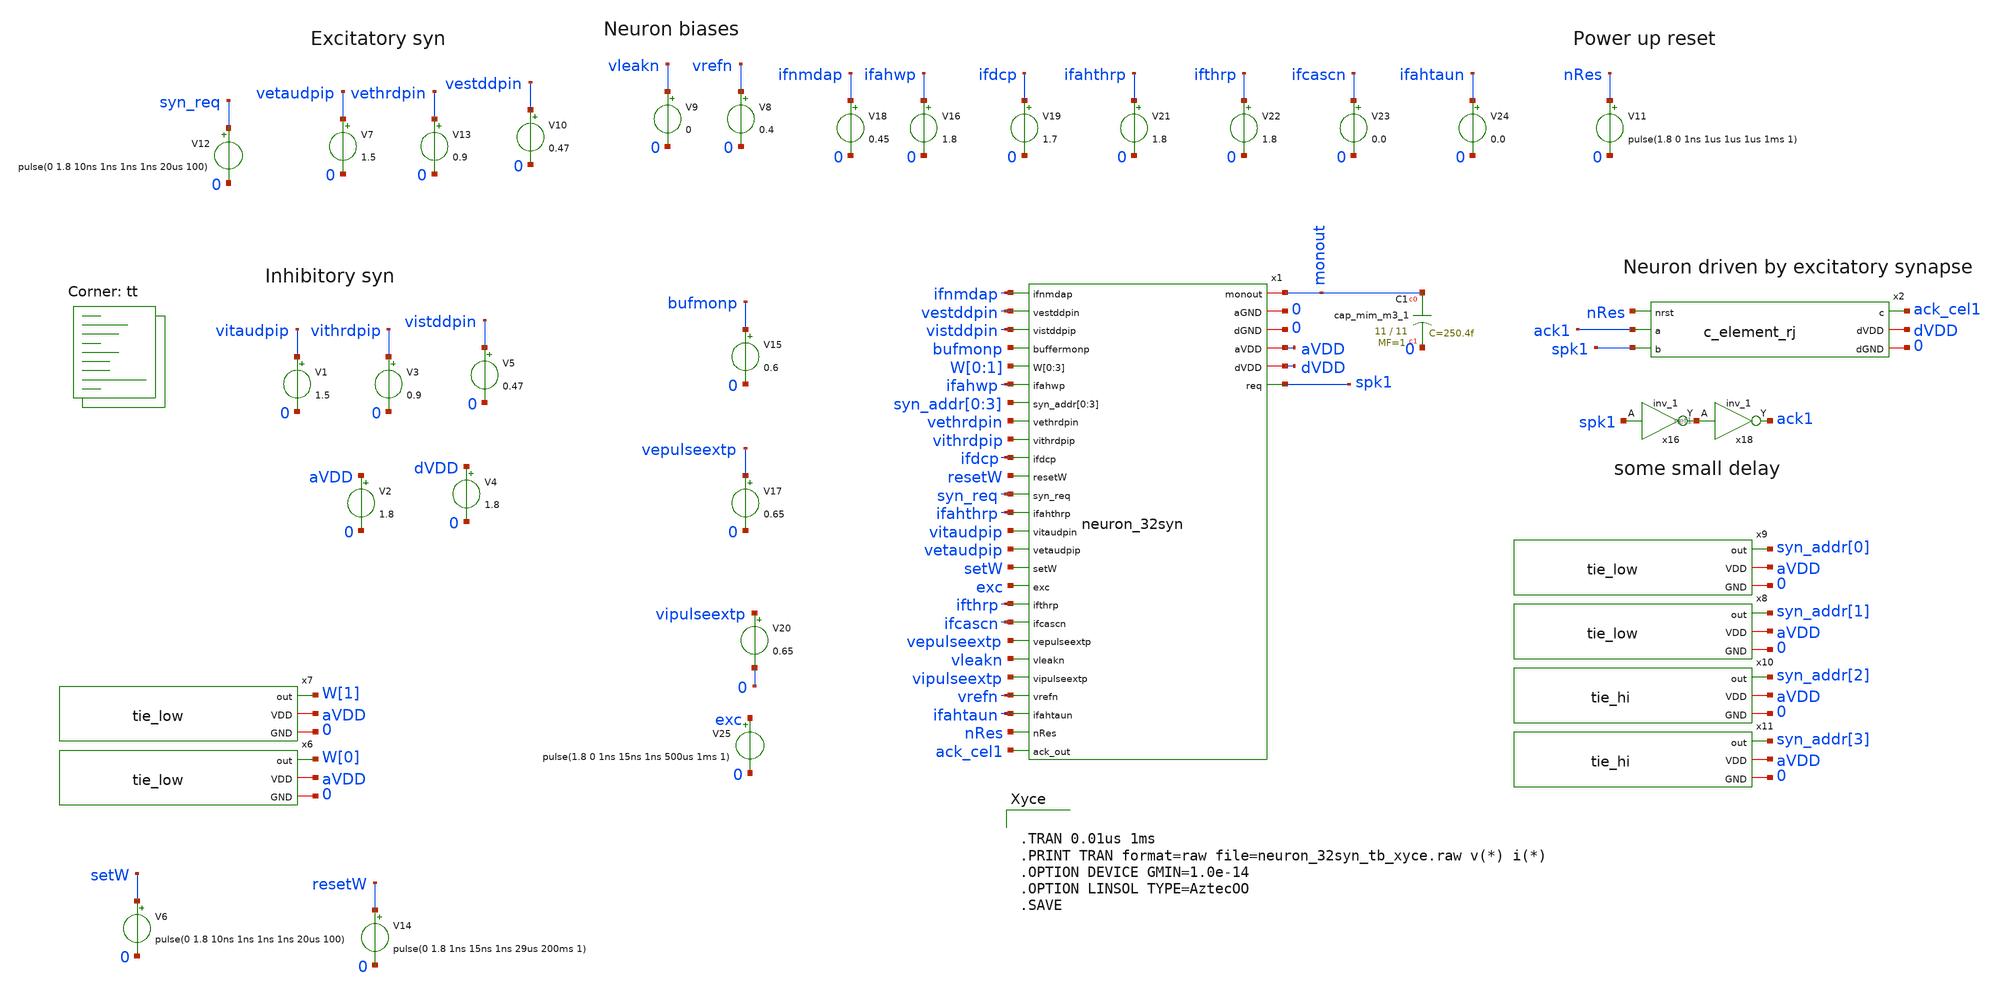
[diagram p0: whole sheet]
** sch_path: design/xschem/neuron_32syn_tb.sch
**.subckt neuron_32syn_tb
V2 aVDD 0 1.8
V8 vrefn 0 0.4
V9 vleakn 0 0
V16 ifahwp 0 1.8
V18 ifnmdap 0 0.45
V19 ifdcp 0 1.7
V21 ifahthrp 0 1.8
V22 ifthrp 0 1.8
V23 ifcascn 0 0.0
V24 ifahtaun 0 0.0
V7 vetaudpip 0 1.5
V13 vethrdpin 0 0.9
V10 vestddpin 0 0.47
V12 syn_req 0 pulse(0 1.8 10ns 1ns 1ns 1ns 20us 100)
V11 nRes 0 pulse(1.8 0 1ns 1us 1us 1us 1ms 1)
x1 ifnmdap vestddpin vistddpin bufmonp W[0] W[1] W[0] W[1] ifahwp syn_addr[0] syn_addr[1]
+ syn_addr[2] syn_addr[3] vethrdpin vithrdpip ifdcp monout resetW syn_req ifahthrp vitaudpip vetaudpip setW exc
+ ifthrp ifcascn vepulseextp vleakn vipulseextp 0 0 vrefn aVDD dVDD ifahtaun nRes ack_cel1 spk1 neuron_32syn
x2 nRes ack1 spk1 ack_cel1 dVDD 0 c_element_rj
V1 vitaudpip 0 1.5
V3 vithrdpip 0 0.9
V5 vistddpin 0 0.47
V15 bufmonp 0 0.6
x6 W[0] aVDD 0 tie_low
x7 W[1] aVDD 0 tie_low
V6 setW 0 pulse(0 1.8 10ns 1ns 1ns 1ns 20us 100)
V14 resetW 0 pulse(0 1.8 1ns 15ns 1ns 29us 200ms 1)
x8 syn_addr[1] aVDD 0 tie_low
x9 syn_addr[0] aVDD 0 tie_low
x10 syn_addr[2] aVDD 0 tie_hi
x11 syn_addr[3] aVDD 0 tie_hi
V17 vepulseextp 0 0.65
V20 vipulseextp 0 0.65
V25 exc 0 pulse(1.8 0 1ns 15ns 1ns 500us 1ms 1)
x16 spk1 0 0 dVDD dVDD net1 sky130_fd_sc_hd__inv_1
x18 net1 0 0 dVDD dVDD ack1 sky130_fd_sc_hd__inv_1
XC1 monout 0 sky130_fd_pr__cap_mim_m3_1 W=11 L=11 MF=1 m=1
V4 dVDD 0 1.8
**** begin user architecture code


* Standard cell simulation files
.include $::SKYWATER_STDCELLS/sky130_fd_sc_hd.spice




.TRAN 0.01us 1ms
.PRINT TRAN format=raw file=neuron_32syn_tb_xyce.raw v(*) i(*)
.OPTION DEVICE GMIN=1.0e-14
.OPTION LINSOL TYPE=AztecOO
.SAVE



.lib $::SKYWATER_MODELS/sky130.lib.spice tt
**** end user architecture code
**.ends

* expanding   symbol:  neuron_32syn.sym # of pins=32
** sym_path: design/xschem/neuron_32syn.sym
** sch_path: design/xschem/neuron_32syn.sch
.subckt neuron_32syn ifnmdap vestddpin vistddpip buffermonp W[0] W[1] W[2] W[3] ifahwp syn_addr[0]
+ syn_addr[1] syn_addr[2] syn_addr[3] vethrdpin vithrdpip ifdcp monout resetW syn_req ifahthrp vitaudpin
+ vetaudpip setW exc ifthrp ifcascn vepulseextp vleakn vipulseextp aGND dGND vrefn aVDD dVDD ifahtaun nRes
+ ack_out req
*.ipin ack_out
*.iopin dGND
*.iopin dVDD
*.ipin vepulseextp
*.ipin syn_addr[0],syn_addr[1],syn_addr[2],syn_addr[3]
*.ipin W[0],W[1],W[2],W[3]
*.ipin vethrdpin
*.ipin vetaudpip
*.ipin vestddpin
*.ipin setW
*.ipin resetW
*.ipin syn_req
*.ipin exc
*.ipin vithrdpip
*.ipin vitaudpin
*.ipin vistddpip
*.ipin vipulseextp
*.opin req
*.ipin vleakn
*.ipin ifdcp
*.ipin ifthrp
*.ipin ifahwp
*.ipin ifahthrp
*.ipin ifahtaun
*.ipin ifcascn
*.ipin vrefn
*.ipin ifnmdap
*.ipin nRes
*.iopin aGND
*.iopin aVDD
*.ipin buffermonp
*.iopin monout
x1 vestddpin net1 W[0] W[1] W[2] W[3] syn_addr[0] syn_addr[1] syn_addr[2] syn_addr[3] vethrdpin
+ resetWe reqe vetaudpip setWe vepulseextp aGND aVDD synapse_array_programmable_16_to_sout
x2 vistddpip net1 W[0] W[1] W[2] W[3] syn_addr[0] syn_addr[1] syn_addr[2] syn_addr[3] vithrdpip
+ resetWi reqi vitaudpin setWi vipulseextp aGND aVDD synapse_array_programmable_inh_16_to_sout
x3 nreq_neu1 net1 net2 ifahwp ifnmdap ifahthrp net3 ifdcp ifthrp ifcascn vleakn vrefn ifahtaun aGND
+ aVDD neuron_analog_fc
x11 nRes req ack_out ack_cel1 dVDD dGND c_element_rj
x4 setW exc dGND dGND dVDD dVDD setWe sky130_fd_sc_hd__and2_1
x5 exc dGND dGND dVDD dVDD nExc sky130_fd_sc_hd__inv_1
x6 setW nExc dGND dGND dVDD dVDD setWi sky130_fd_sc_hd__and2_1
x7 resetW exc dGND dGND dVDD dVDD resetWe sky130_fd_sc_hd__and2_1
x8 resetW nExc dGND dGND dVDD dVDD resetWi sky130_fd_sc_hd__and2_1
x10 syn_req exc dGND dGND dVDD dVDD reqe sky130_fd_sc_hd__and2_1
x12 syn_req nExc dGND dGND dVDD dVDD reqi sky130_fd_sc_hd__and2_1
x13 monout buffermonp net3 aGND aVDD buffer_mon
x14 ack_cel1 dGND dGND dVDD dVDD net2 sky130_fd_sc_hd__inv_1
x15 nreq_neu1 req dVDD dGND schmitt_trigger
.ends


* expanding   symbol:  c_element_rj.sym # of pins=6
** sym_path: design/xschem/c_element_rj.sym
** sch_path: design/xschem/c_element_rj.sch
.subckt c_element_rj nrst a b c dVDD dGND
*.iopin dGND
*.iopin dVDD
*.opin c
*.ipin b
*.ipin a
*.ipin nrst
XM14 c net6 dVDD dVDD sky130_fd_pr__pfet_01v8 L=0.15 W=1 nf=1 ad='int((nf+1)/2) * W/nf * 0.29' as='int((nf+2)/2) * W/nf * 0.29'
+ pd='2*int((nf+1)/2) * (W/nf + 0.29)' ps='2*int((nf+2)/2) * (W/nf + 0.29)' nrd='0.29 / W' nrs='0.29 / W'
+ sa=0 sb=0 sd=0 mult=1 m=1
XM5 net6 nrst dVDD dVDD sky130_fd_pr__pfet_01v8 L=0.15 W=1 nf=1 ad='int((nf+1)/2) * W/nf * 0.29' as='int((nf+2)/2) * W/nf * 0.29'
+ pd='2*int((nf+1)/2) * (W/nf + 0.29)' ps='2*int((nf+2)/2) * (W/nf + 0.29)' nrd='0.29 / W' nrs='0.29 / W'
+ sa=0 sb=0 sd=0 mult=1 m=1
XM6 net5 b dVDD dVDD sky130_fd_pr__pfet_01v8 L=0.15 W=1 nf=1 ad='int((nf+1)/2) * W/nf * 0.29' as='int((nf+2)/2) * W/nf * 0.29'
+ pd='2*int((nf+1)/2) * (W/nf + 0.29)' ps='2*int((nf+2)/2) * (W/nf + 0.29)' nrd='0.29 / W' nrs='0.29 / W'
+ sa=0 sb=0 sd=0 mult=1 m=1
XM4 net4 a dVDD dVDD sky130_fd_pr__pfet_01v8 L=0.15 W=1 nf=1 ad='int((nf+1)/2) * W/nf * 0.29' as='int((nf+2)/2) * W/nf * 0.29'
+ pd='2*int((nf+1)/2) * (W/nf + 0.29)' ps='2*int((nf+2)/2) * (W/nf + 0.29)' nrd='0.29 / W' nrs='0.29 / W'
+ sa=0 sb=0 sd=0 mult=1 m=1
XM7 net3 b net4 dVDD sky130_fd_pr__pfet_01v8 L=0.15 W=1 nf=1 ad='int((nf+1)/2) * W/nf * 0.29' as='int((nf+2)/2) * W/nf * 0.29'
+ pd='2*int((nf+1)/2) * (W/nf + 0.29)' ps='2*int((nf+2)/2) * (W/nf + 0.29)' nrd='0.29 / W' nrs='0.29 / W'
+ sa=0 sb=0 sd=0 mult=1 m=1
XM8 net3 a net5 dVDD sky130_fd_pr__pfet_01v8 L=0.15 W=1 nf=1 ad='int((nf+1)/2) * W/nf * 0.29' as='int((nf+2)/2) * W/nf * 0.29'
+ pd='2*int((nf+1)/2) * (W/nf + 0.29)' ps='2*int((nf+2)/2) * (W/nf + 0.29)' nrd='0.29 / W' nrs='0.29 / W'
+ sa=0 sb=0 sd=0 mult=1 m=1
XM10 net5 c net4 dVDD sky130_fd_pr__pfet_01v8 L=0.15 W=1 nf=1 ad='int((nf+1)/2) * W/nf * 0.29' as='int((nf+2)/2) * W/nf * 0.29'
+ pd='2*int((nf+1)/2) * (W/nf + 0.29)' ps='2*int((nf+2)/2) * (W/nf + 0.29)' nrd='0.29 / W' nrs='0.29 / W'
+ sa=0 sb=0 sd=0 mult=1 m=1
XM12 c net6 dGND dGND sky130_fd_pr__nfet_01v8 L=0.15 W=0.65 nf=1 ad='int((nf+1)/2) * W/nf * 0.29' as='int((nf+2)/2) * W/nf * 0.29'
+ pd='2*int((nf+1)/2) * (W/nf + 0.29)' ps='2*int((nf+2)/2) * (W/nf + 0.29)' nrd='0.29 / W' nrs='0.29 / W'
+ sa=0 sb=0 sd=0 mult=1 m=1
XM1 net3 nrst net6 dGND sky130_fd_pr__nfet_01v8 L=0.15 W=0.65 nf=1 ad='int((nf+1)/2) * W/nf * 0.29' as='int((nf+2)/2) * W/nf * 0.29'
+ pd='2*int((nf+1)/2) * (W/nf + 0.29)' ps='2*int((nf+2)/2) * (W/nf + 0.29)' nrd='0.29 / W' nrs='0.29 / W'
+ sa=0 sb=0 sd=0 mult=1 m=1
XM2 net3 b net1 dGND sky130_fd_pr__nfet_01v8 L=0.15 W=0.65 nf=1 ad='int((nf+1)/2) * W/nf * 0.29' as='int((nf+2)/2) * W/nf * 0.29'
+ pd='2*int((nf+1)/2) * (W/nf + 0.29)' ps='2*int((nf+2)/2) * (W/nf + 0.29)' nrd='0.29 / W' nrs='0.29 / W'
+ sa=0 sb=0 sd=0 mult=1 m=1
XM3 net3 a net2 dGND sky130_fd_pr__nfet_01v8 L=0.15 W=0.65 nf=1 ad='int((nf+1)/2) * W/nf * 0.29' as='int((nf+2)/2) * W/nf * 0.29'
+ pd='2*int((nf+1)/2) * (W/nf + 0.29)' ps='2*int((nf+2)/2) * (W/nf + 0.29)' nrd='0.29 / W' nrs='0.29 / W'
+ sa=0 sb=0 sd=0 mult=1 m=1
XM9 net2 c net1 dGND sky130_fd_pr__nfet_01v8 L=0.15 W=0.65 nf=1 ad='int((nf+1)/2) * W/nf * 0.29' as='int((nf+2)/2) * W/nf * 0.29'
+ pd='2*int((nf+1)/2) * (W/nf + 0.29)' ps='2*int((nf+2)/2) * (W/nf + 0.29)' nrd='0.29 / W' nrs='0.29 / W'
+ sa=0 sb=0 sd=0 mult=1 m=1
XM11 net1 a dGND dGND sky130_fd_pr__nfet_01v8 L=0.15 W=0.65 nf=1 ad='int((nf+1)/2) * W/nf * 0.29' as='int((nf+2)/2) * W/nf * 0.29'
+ pd='2*int((nf+1)/2) * (W/nf + 0.29)' ps='2*int((nf+2)/2) * (W/nf + 0.29)' nrd='0.29 / W' nrs='0.29 / W'
+ sa=0 sb=0 sd=0 mult=1 m=1
XM13 net2 b dGND dGND sky130_fd_pr__nfet_01v8 L=0.15 W=0.65 nf=1 ad='int((nf+1)/2) * W/nf * 0.29' as='int((nf+2)/2) * W/nf * 0.29'
+ pd='2*int((nf+1)/2) * (W/nf + 0.29)' ps='2*int((nf+2)/2) * (W/nf + 0.29)' nrd='0.29 / W' nrs='0.29 / W'
+ sa=0 sb=0 sd=0 mult=1 m=1
.ends


* expanding   symbol:  tie_low.sym # of pins=3
** sym_path: design/xschem/tie_low.sym
** sch_path: design/xschem/tie_low.sch
.subckt tie_low out VDD GND
*.iopin VDD
*.iopin GND
*.opin out
XM4 net1 net1 VDD VDD sky130_fd_pr__pfet_01v8 L=0.15 W=1 nf=1 ad='int((nf+1)/2) * W/nf * 0.29' as='int((nf+2)/2) * W/nf * 0.29'
+ pd='2*int((nf+1)/2) * (W/nf + 0.29)' ps='2*int((nf+2)/2) * (W/nf + 0.29)' nrd='0.29 / W' nrs='0.29 / W'
+ sa=0 sb=0 sd=0 mult=1 m=1
XM2 out net1 GND GND sky130_fd_pr__nfet_01v8 L=0.15 W=0.65 nf=1 ad='int((nf+1)/2) * W/nf * 0.29' as='int((nf+2)/2) * W/nf * 0.29'
+ pd='2*int((nf+1)/2) * (W/nf + 0.29)' ps='2*int((nf+2)/2) * (W/nf + 0.29)' nrd='0.29 / W' nrs='0.29 / W'
+ sa=0 sb=0 sd=0 mult=1 m=1
.ends


* expanding   symbol:  tie_hi.sym # of pins=3
** sym_path: design/xschem/tie_hi.sym
** sch_path: design/xschem/tie_hi.sch
.subckt tie_hi out VDD GND
*.iopin VDD
*.iopin GND
*.opin out
XM4 out net1 VDD VDD sky130_fd_pr__pfet_01v8 L=0.15 W=1 nf=1 ad='int((nf+1)/2) * W/nf * 0.29' as='int((nf+2)/2) * W/nf * 0.29'
+ pd='2*int((nf+1)/2) * (W/nf + 0.29)' ps='2*int((nf+2)/2) * (W/nf + 0.29)' nrd='0.29 / W' nrs='0.29 / W'
+ sa=0 sb=0 sd=0 mult=1 m=1
XM2 net1 net1 GND GND sky130_fd_pr__nfet_01v8 L=0.15 W=0.65 nf=1 ad='int((nf+1)/2) * W/nf * 0.29' as='int((nf+2)/2) * W/nf * 0.29'
+ pd='2*int((nf+1)/2) * (W/nf + 0.29)' ps='2*int((nf+2)/2) * (W/nf + 0.29)' nrd='0.29 / W' nrs='0.29 / W'
+ sa=0 sb=0 sd=0 mult=1 m=1
.ends


* expanding   symbol:  synapse_array_programmable_16_to_sout.sym # of pins=12
** sym_path: design/xschem/synapse_array_programmable_16_to_sout.sym
** sch_path: design/xschem/synapse_array_programmable_16_to_sout.sch
.subckt synapse_array_programmable_16_to_sout vstddpin sout W[0] W[1] W[2] W[3] syn_addr[0]
+ syn_addr[1] syn_addr[2] syn_addr[3] vthrdpin resetW req vtaudpip setW vpulseextp GND VDD
*.iopin GND
*.iopin VDD
*.ipin vpulseextp
*.ipin syn_addr[0],syn_addr[1],syn_addr[2],syn_addr[3]
*.ipin W[0],W[1],W[2],W[3]
*.ipin vthrdpin
*.ipin vtaudpip
*.ipin vstddpin
*.iopin sout
*.ipin setW
*.ipin resetW
*.ipin req
x1[0] sout vstddpin net1[15] resetW vthrdpin setW vtaudpip W[0] W[1] W[2] W[3] vpulseextp GND VDD
+ synapse_4bit_memory
x1[1] sout vstddpin net1[14] resetW vthrdpin setW vtaudpip W[0] W[1] W[2] W[3] vpulseextp GND VDD
+ synapse_4bit_memory
x1[2] sout vstddpin net1[13] resetW vthrdpin setW vtaudpip W[0] W[1] W[2] W[3] vpulseextp GND VDD
+ synapse_4bit_memory
x1[3] sout vstddpin net1[12] resetW vthrdpin setW vtaudpip W[0] W[1] W[2] W[3] vpulseextp GND VDD
+ synapse_4bit_memory
x1[4] sout vstddpin net1[11] resetW vthrdpin setW vtaudpip W[0] W[1] W[2] W[3] vpulseextp GND VDD
+ synapse_4bit_memory
x1[5] sout vstddpin net1[10] resetW vthrdpin setW vtaudpip W[0] W[1] W[2] W[3] vpulseextp GND VDD
+ synapse_4bit_memory
x1[6] sout vstddpin net1[9] resetW vthrdpin setW vtaudpip W[0] W[1] W[2] W[3] vpulseextp GND VDD
+ synapse_4bit_memory
x1[7] sout vstddpin net1[8] resetW vthrdpin setW vtaudpip W[0] W[1] W[2] W[3] vpulseextp GND VDD
+ synapse_4bit_memory
x1[8] sout vstddpin net1[7] resetW vthrdpin setW vtaudpip W[0] W[1] W[2] W[3] vpulseextp GND VDD
+ synapse_4bit_memory
x1[9] sout vstddpin net1[6] resetW vthrdpin setW vtaudpip W[0] W[1] W[2] W[3] vpulseextp GND VDD
+ synapse_4bit_memory
x1[10] sout vstddpin net1[5] resetW vthrdpin setW vtaudpip W[0] W[1] W[2] W[3] vpulseextp GND VDD
+ synapse_4bit_memory
x1[11] sout vstddpin net1[4] resetW vthrdpin setW vtaudpip W[0] W[1] W[2] W[3] vpulseextp GND VDD
+ synapse_4bit_memory
x1[12] sout vstddpin net1[3] resetW vthrdpin setW vtaudpip W[0] W[1] W[2] W[3] vpulseextp GND VDD
+ synapse_4bit_memory
x1[13] sout vstddpin net1[2] resetW vthrdpin setW vtaudpip W[0] W[1] W[2] W[3] vpulseextp GND VDD
+ synapse_4bit_memory
x1[14] sout vstddpin net1[1] resetW vthrdpin setW vtaudpip W[0] W[1] W[2] W[3] vpulseextp GND VDD
+ synapse_4bit_memory
x1[15] sout vstddpin net1[0] resetW vthrdpin setW vtaudpip W[0] W[1] W[2] W[3] vpulseextp GND VDD
+ synapse_4bit_memory
x3 syn_addr[0] syn_addr[1] syn_addr[2] syn_addr[3] D[15] D[14] D[13] D[12] D[11] D[10] D[9] D[8]
+ D[7] D[6] D[5] D[4] D[3] D[2] D[1] D[0] req req_syn VDD GND decoder_4_to_16
x4[0] D[0] req_syn GND GND VDD VDD net1[15] sky130_fd_sc_hd__and2_1
x4[1] D[1] req_syn GND GND VDD VDD net1[14] sky130_fd_sc_hd__and2_1
x4[2] D[2] req_syn GND GND VDD VDD net1[13] sky130_fd_sc_hd__and2_1
x4[3] D[3] req_syn GND GND VDD VDD net1[12] sky130_fd_sc_hd__and2_1
x4[4] D[4] req_syn GND GND VDD VDD net1[11] sky130_fd_sc_hd__and2_1
x4[5] D[5] req_syn GND GND VDD VDD net1[10] sky130_fd_sc_hd__and2_1
x4[6] D[6] req_syn GND GND VDD VDD net1[9] sky130_fd_sc_hd__and2_1
x4[7] D[7] req_syn GND GND VDD VDD net1[8] sky130_fd_sc_hd__and2_1
x4[8] D[8] req_syn GND GND VDD VDD net1[7] sky130_fd_sc_hd__and2_1
x4[9] D[9] req_syn GND GND VDD VDD net1[6] sky130_fd_sc_hd__and2_1
x4[10] D[10] req_syn GND GND VDD VDD net1[5] sky130_fd_sc_hd__and2_1
x4[11] D[11] req_syn GND GND VDD VDD net1[4] sky130_fd_sc_hd__and2_1
x4[12] D[12] req_syn GND GND VDD VDD net1[3] sky130_fd_sc_hd__and2_1
x4[13] D[13] req_syn GND GND VDD VDD net1[2] sky130_fd_sc_hd__and2_1
x4[14] D[14] req_syn GND GND VDD VDD net1[1] sky130_fd_sc_hd__and2_1
x4[15] D[15] req_syn GND GND VDD VDD net1[0] sky130_fd_sc_hd__and2_1
.ends


* expanding   symbol:  synapse_array_programmable_inh_16_to_sout.sym # of pins=12
** sym_path: design/xschem/synapse_array_programmable_inh_16_to_sout.sym
** sch_path: design/xschem/synapse_array_programmable_inh_16_to_sout.sch
.subckt synapse_array_programmable_inh_16_to_sout vstddpip sout W[0] W[1] W[2] W[3] syn_addr[0]
+ syn_addr[1] syn_addr[2] syn_addr[3] vthrdpip resetW req vtaudpin setW vpulseextp GND VDD
*.iopin GND
*.iopin VDD
*.ipin vpulseextp
*.ipin syn_addr[0],syn_addr[1],syn_addr[2],syn_addr[3]
*.ipin W[0],W[1],W[2],W[3]
*.ipin vthrdpip
*.ipin vtaudpin
*.ipin vstddpip
*.iopin sout
*.ipin setW
*.ipin resetW
*.ipin req
x3 syn_addr[0] syn_addr[1] syn_addr[2] syn_addr[3] D[15] D[14] D[13] D[12] D[11] D[10] D[9] D[8]
+ D[7] D[6] D[5] D[4] D[3] D[2] D[1] D[0] req req_syn VDD GND decoder_4_to_16
x4[0] D[0] req_syn GND GND VDD VDD net1[15] sky130_fd_sc_hd__and2_1
x4[1] D[1] req_syn GND GND VDD VDD net1[14] sky130_fd_sc_hd__and2_1
x4[2] D[2] req_syn GND GND VDD VDD net1[13] sky130_fd_sc_hd__and2_1
x4[3] D[3] req_syn GND GND VDD VDD net1[12] sky130_fd_sc_hd__and2_1
x4[4] D[4] req_syn GND GND VDD VDD net1[11] sky130_fd_sc_hd__and2_1
x4[5] D[5] req_syn GND GND VDD VDD net1[10] sky130_fd_sc_hd__and2_1
x4[6] D[6] req_syn GND GND VDD VDD net1[9] sky130_fd_sc_hd__and2_1
x4[7] D[7] req_syn GND GND VDD VDD net1[8] sky130_fd_sc_hd__and2_1
x4[8] D[8] req_syn GND GND VDD VDD net1[7] sky130_fd_sc_hd__and2_1
x4[9] D[9] req_syn GND GND VDD VDD net1[6] sky130_fd_sc_hd__and2_1
x4[10] D[10] req_syn GND GND VDD VDD net1[5] sky130_fd_sc_hd__and2_1
x4[11] D[11] req_syn GND GND VDD VDD net1[4] sky130_fd_sc_hd__and2_1
x4[12] D[12] req_syn GND GND VDD VDD net1[3] sky130_fd_sc_hd__and2_1
x4[13] D[13] req_syn GND GND VDD VDD net1[2] sky130_fd_sc_hd__and2_1
x4[14] D[14] req_syn GND GND VDD VDD net1[1] sky130_fd_sc_hd__and2_1
x4[15] D[15] req_syn GND GND VDD VDD net1[0] sky130_fd_sc_hd__and2_1
x1[0] sout vstddpip net1[15] resetW vthrdpip setW vtaudpin W[0] W[1] W[2] W[3] vpulseextp GND VDD
+ synapse_4bit_memory_inh
x1[1] sout vstddpip net1[14] resetW vthrdpip setW vtaudpin W[0] W[1] W[2] W[3] vpulseextp GND VDD
+ synapse_4bit_memory_inh
x1[2] sout vstddpip net1[13] resetW vthrdpip setW vtaudpin W[0] W[1] W[2] W[3] vpulseextp GND VDD
+ synapse_4bit_memory_inh
x1[3] sout vstddpip net1[12] resetW vthrdpip setW vtaudpin W[0] W[1] W[2] W[3] vpulseextp GND VDD
+ synapse_4bit_memory_inh
x1[4] sout vstddpip net1[11] resetW vthrdpip setW vtaudpin W[0] W[1] W[2] W[3] vpulseextp GND VDD
+ synapse_4bit_memory_inh
x1[5] sout vstddpip net1[10] resetW vthrdpip setW vtaudpin W[0] W[1] W[2] W[3] vpulseextp GND VDD
+ synapse_4bit_memory_inh
x1[6] sout vstddpip net1[9] resetW vthrdpip setW vtaudpin W[0] W[1] W[2] W[3] vpulseextp GND VDD
+ synapse_4bit_memory_inh
x1[7] sout vstddpip net1[8] resetW vthrdpip setW vtaudpin W[0] W[1] W[2] W[3] vpulseextp GND VDD
+ synapse_4bit_memory_inh
x1[8] sout vstddpip net1[7] resetW vthrdpip setW vtaudpin W[0] W[1] W[2] W[3] vpulseextp GND VDD
+ synapse_4bit_memory_inh
x1[9] sout vstddpip net1[6] resetW vthrdpip setW vtaudpin W[0] W[1] W[2] W[3] vpulseextp GND VDD
+ synapse_4bit_memory_inh
x1[10] sout vstddpip net1[5] resetW vthrdpip setW vtaudpin W[0] W[1] W[2] W[3] vpulseextp GND VDD
+ synapse_4bit_memory_inh
x1[11] sout vstddpip net1[4] resetW vthrdpip setW vtaudpin W[0] W[1] W[2] W[3] vpulseextp GND VDD
+ synapse_4bit_memory_inh
x1[12] sout vstddpip net1[3] resetW vthrdpip setW vtaudpin W[0] W[1] W[2] W[3] vpulseextp GND VDD
+ synapse_4bit_memory_inh
x1[13] sout vstddpip net1[2] resetW vthrdpip setW vtaudpin W[0] W[1] W[2] W[3] vpulseextp GND VDD
+ synapse_4bit_memory_inh
x1[14] sout vstddpip net1[1] resetW vthrdpip setW vtaudpin W[0] W[1] W[2] W[3] vpulseextp GND VDD
+ synapse_4bit_memory_inh
x1[15] sout vstddpip net1[0] resetW vthrdpip setW vtaudpin W[0] W[1] W[2] W[3] vpulseextp GND VDD
+ synapse_4bit_memory_inh
.ends


* expanding   symbol:  neuron_analog_fc.sym # of pins=15
** sym_path: design/xschem/neuron_analog_fc.sym
** sch_path: design/xschem/neuron_analog_fc.sch
.subckt neuron_analog_fc nreq sinp nack ifahwp ifnmdap ifahthrp vmem ifdcp ifthrp ifcascn vleakn
+ vrefn ifahtaun GND VDD
*.ipin vleakn
*.iopin GND
*.iopin VDD
*.opin nreq
*.ipin vrefn
*.ipin nack
*.ipin ifdcp
*.ipin ifthrp
*.ipin ifnmdap
*.ipin ifahwp
*.ipin ifahthrp
*.ipin ifahtaun
*.ipin ifcascn
*.iopin vmem
*.iopin sinp
XC1 GND vmem sky130_fd_pr__cap_mim_m3_1 W=11 L=11 MF=1 m=1
XM8 net4 vrefn GND GND sky130_fd_pr__nfet_01v8 L=0.25 W=0.8 nf=1 ad='int((nf+1)/2) * W/nf * 0.29' as='int((nf+2)/2) * W/nf * 0.29'
+ pd='2*int((nf+1)/2) * (W/nf + 0.29)' ps='2*int((nf+2)/2) * (W/nf + 0.29)' nrd='0.29 / W' nrs='0.29 / W'
+ sa=0 sb=0 sd=0 mult=1 m=1
XM9 net5 nack VDD VDD sky130_fd_pr__pfet_01v8 L=0.2 W=1.2 nf=1 ad='int((nf+1)/2) * W/nf * 0.29' as='int((nf+2)/2) * W/nf * 0.29'
+ pd='2*int((nf+1)/2) * (W/nf + 0.29)' ps='2*int((nf+2)/2) * (W/nf + 0.29)' nrd='0.29 / W' nrs='0.29 / W'
+ sa=0 sb=0 sd=0 mult=1 m=1
XC2 GND net3 sky130_fd_pr__cap_mim_m3_1 W=4 L=2 MF=1 m=1
XM21 vmem net3 GND GND sky130_fd_pr__nfet_01v8 L=0.25 W=1 nf=1 ad='int((nf+1)/2) * W/nf * 0.29' as='int((nf+2)/2) * W/nf * 0.29'
+ pd='2*int((nf+1)/2) * (W/nf + 0.29)' ps='2*int((nf+2)/2) * (W/nf + 0.29)' nrd='0.29 / W' nrs='0.29 / W'
+ sa=0 sb=0 sd=0 mult=1 m=1
XM15 net12 ifnmdap sinp VDD sky130_fd_pr__pfet_01v8 L=0.15 W=1 nf=1 ad='int((nf+1)/2) * W/nf * 0.29'
+ as='int((nf+2)/2) * W/nf * 0.29' pd='2*int((nf+1)/2) * (W/nf + 0.29)' ps='2*int((nf+2)/2) * (W/nf + 0.29)'
+ nrd='0.29 / W' nrs='0.29 / W' sa=0 sb=0 sd=0 mult=1 m=1
XC3 GND net8 sky130_fd_pr__cap_mim_m3_1 W=5 L=5 MF=1 m=1
XM12 GND vmem sinp VDD sky130_fd_pr__pfet_01v8 L=0.15 W=1 nf=1 ad='int((nf+1)/2) * W/nf * 0.29' as='int((nf+2)/2) * W/nf * 0.29'
+ pd='2*int((nf+1)/2) * (W/nf + 0.29)' ps='2*int((nf+2)/2) * (W/nf + 0.29)' nrd='0.29 / W' nrs='0.29 / W'
+ sa=0 sb=0 sd=0 mult=1 m=1
XM11 GND ifthrp net6 VDD sky130_fd_pr__pfet_01v8 L=0.15 W=1 nf=1 ad='int((nf+1)/2) * W/nf * 0.29' as='int((nf+2)/2) * W/nf * 0.29'
+ pd='2*int((nf+1)/2) * (W/nf + 0.29)' ps='2*int((nf+2)/2) * (W/nf + 0.29)' nrd='0.29 / W' nrs='0.29 / W'
+ sa=0 sb=0 sd=0 mult=1 m=1
XM16 net7 nack VDD VDD sky130_fd_pr__pfet_01v8 L=0.15 W=1 nf=1 ad='int((nf+1)/2) * W/nf * 0.29' as='int((nf+2)/2) * W/nf * 0.29'
+ pd='2*int((nf+1)/2) * (W/nf + 0.29)' ps='2*int((nf+2)/2) * (W/nf + 0.29)' nrd='0.29 / W' nrs='0.29 / W'
+ sa=0 sb=0 sd=0 mult=1 m=1
XM17 net9 ifahwp net7 VDD sky130_fd_pr__pfet_01v8 L=0.15 W=1 nf=1 ad='int((nf+1)/2) * W/nf * 0.29' as='int((nf+2)/2) * W/nf * 0.29'
+ pd='2*int((nf+1)/2) * (W/nf + 0.29)' ps='2*int((nf+2)/2) * (W/nf + 0.29)' nrd='0.29 / W' nrs='0.29 / W'
+ sa=0 sb=0 sd=0 mult=1 m=1
XM18 GND ifahthrp net9 VDD sky130_fd_pr__pfet_01v8 L=0.15 W=1 nf=1 ad='int((nf+1)/2) * W/nf * 0.29' as='int((nf+2)/2) * W/nf * 0.29'
+ pd='2*int((nf+1)/2) * (W/nf + 0.29)' ps='2*int((nf+2)/2) * (W/nf + 0.29)' nrd='0.29 / W' nrs='0.29 / W'
+ sa=0 sb=0 sd=0 mult=1 m=1
XM19 net8 net8 net9 VDD sky130_fd_pr__pfet_01v8 L=0.15 W=1 nf=1 ad='int((nf+1)/2) * W/nf * 0.29' as='int((nf+2)/2) * W/nf * 0.29'
+ pd='2*int((nf+1)/2) * (W/nf + 0.29)' ps='2*int((nf+2)/2) * (W/nf + 0.29)' nrd='0.29 / W' nrs='0.29 / W'
+ sa=0 sb=0 sd=0 mult=1 m=1
XM1 net11 ifdcp VDD VDD sky130_fd_pr__pfet_01v8 L=0.3 W=1 nf=1 ad='int((nf+1)/2) * W/nf * 0.29' as='int((nf+2)/2) * W/nf * 0.29'
+ pd='2*int((nf+1)/2) * (W/nf + 0.29)' ps='2*int((nf+2)/2) * (W/nf + 0.29)' nrd='0.29 / W' nrs='0.29 / W'
+ sa=0 sb=0 sd=0 mult=1 m=1
XM5 net2 nreq VDD VDD sky130_fd_pr__pfet_01v8 L=0.15 W=1 nf=1 ad='int((nf+1)/2) * W/nf * 0.29' as='int((nf+2)/2) * W/nf * 0.29'
+ pd='2*int((nf+1)/2) * (W/nf + 0.29)' ps='2*int((nf+2)/2) * (W/nf + 0.29)' nrd='0.29 / W' nrs='0.29 / W'
+ sa=0 sb=0 sd=0 mult=1 m=1
XM6 nreq vmem net2 VDD sky130_fd_pr__pfet_01v8 L=0.15 W=1 nf=1 ad='int((nf+1)/2) * W/nf * 0.29' as='int((nf+2)/2) * W/nf * 0.29'
+ pd='2*int((nf+1)/2) * (W/nf + 0.29)' ps='2*int((nf+2)/2) * (W/nf + 0.29)' nrd='0.29 / W' nrs='0.29 / W'
+ sa=0 sb=0 sd=0 mult=1 m=1
XM10 net3 nreq net5 VDD sky130_fd_pr__pfet_01v8 L=0.15 W=1 nf=1 ad='int((nf+1)/2) * W/nf * 0.29' as='int((nf+2)/2) * W/nf * 0.29'
+ pd='2*int((nf+1)/2) * (W/nf + 0.29)' ps='2*int((nf+2)/2) * (W/nf + 0.29)' nrd='0.29 / W' nrs='0.29 / W'
+ sa=0 sb=0 sd=0 mult=1 m=1
XM2 nreq vmem net1 GND sky130_fd_pr__nfet_01v8 L=0.15 W=0.65 nf=1 ad='int((nf+1)/2) * W/nf * 0.29' as='int((nf+2)/2) * W/nf * 0.29'
+ pd='2*int((nf+1)/2) * (W/nf + 0.29)' ps='2*int((nf+2)/2) * (W/nf + 0.29)' nrd='0.29 / W' nrs='0.29 / W'
+ sa=0 sb=0 sd=0 mult=1 m=1
XM3 net1 net1 GND GND sky130_fd_pr__nfet_01v8 L=0.15 W=0.65 nf=1 ad='int((nf+1)/2) * W/nf * 0.29' as='int((nf+2)/2) * W/nf * 0.29'
+ pd='2*int((nf+1)/2) * (W/nf + 0.29)' ps='2*int((nf+2)/2) * (W/nf + 0.29)' nrd='0.29 / W' nrs='0.29 / W'
+ sa=0 sb=0 sd=0 mult=1 m=1
XM7 net3 nreq net4 GND sky130_fd_pr__nfet_01v8 L=0.15 W=0.65 nf=1 ad='int((nf+1)/2) * W/nf * 0.29' as='int((nf+2)/2) * W/nf * 0.29'
+ pd='2*int((nf+1)/2) * (W/nf + 0.29)' ps='2*int((nf+2)/2) * (W/nf + 0.29)' nrd='0.29 / W' nrs='0.29 / W'
+ sa=0 sb=0 sd=0 mult=1 m=1
XM14 vmem vleakn net13 GND sky130_fd_pr__nfet_01v8 L=0.15 W=0.65 nf=1 ad='int((nf+1)/2) * W/nf * 0.29'
+ as='int((nf+2)/2) * W/nf * 0.29' pd='2*int((nf+1)/2) * (W/nf + 0.29)' ps='2*int((nf+2)/2) * (W/nf + 0.29)'
+ nrd='0.29 / W' nrs='0.29 / W' sa=0 sb=0 sd=0 mult=1 m=1
XM4 vmem nreq VDD VDD sky130_fd_pr__pfet_01v8 L=0.15 W=1 nf=1 ad='int((nf+1)/2) * W/nf * 0.29' as='int((nf+2)/2) * W/nf * 0.29'
+ pd='2*int((nf+1)/2) * (W/nf + 0.29)' ps='2*int((nf+2)/2) * (W/nf + 0.29)' nrd='0.29 / W' nrs='0.29 / W'
+ sa=0 sb=0 sd=0 mult=1 m=1
XM24 vmem vmem net6 VDD sky130_fd_pr__pfet_01v8 L=0.15 W=1 nf=1 ad='int((nf+1)/2) * W/nf * 0.29' as='int((nf+2)/2) * W/nf * 0.29'
+ pd='2*int((nf+1)/2) * (W/nf + 0.29)' ps='2*int((nf+2)/2) * (W/nf + 0.29)' nrd='0.29 / W' nrs='0.29 / W'
+ sa=0 sb=0 sd=0 mult=1 m=1
Vmeas net11 net6 0
.save i(vmeas)
Vmeas1 net13 GND 0
.save i(vmeas1)
XM13 net6 ifcascn net10 GND sky130_fd_pr__nfet_01v8 L=0.15 W=0.65 nf=1 ad='int((nf+1)/2) * W/nf * 0.29'
+ as='int((nf+2)/2) * W/nf * 0.29' pd='2*int((nf+1)/2) * (W/nf + 0.29)' ps='2*int((nf+2)/2) * (W/nf + 0.29)'
+ nrd='0.29 / W' nrs='0.29 / W' sa=0 sb=0 sd=0 mult=1 m=1
XM20 net10 net8 GND GND sky130_fd_pr__nfet_01v8 L=0.15 W=0.65 nf=1 ad='int((nf+1)/2) * W/nf * 0.29' as='int((nf+2)/2) * W/nf * 0.29'
+ pd='2*int((nf+1)/2) * (W/nf + 0.29)' ps='2*int((nf+2)/2) * (W/nf + 0.29)' nrd='0.29 / W' nrs='0.29 / W'
+ sa=0 sb=0 sd=0 mult=1 m=1
XM22 net8 ifahtaun GND GND sky130_fd_pr__nfet_01v8 L=0.15 W=0.65 nf=1 ad='int((nf+1)/2) * W/nf * 0.29'
+ as='int((nf+2)/2) * W/nf * 0.29' pd='2*int((nf+1)/2) * (W/nf + 0.29)' ps='2*int((nf+2)/2) * (W/nf + 0.29)'
+ nrd='0.29 / W' nrs='0.29 / W' sa=0 sb=0 sd=0 mult=1 m=1
.ends


* expanding   symbol:  buffer_mon.sym # of pins=5
** sym_path: design/xschem/buffer_mon.sym
** sch_path: design/xschem/buffer_mon.sch
.subckt buffer_mon out mon buf_n AGND AVDD
*.iopin AGND
*.iopin AVDD
*.ipin buf_n
*.ipin mon
*.opin out
XM1 net2 net2 AVDD AVDD sky130_fd_pr__pfet_01v8 L=1.0 W=1.0 nf=1 ad='int((nf+1)/2) * W/nf * 0.29' as='int((nf+2)/2) * W/nf * 0.29'
+ pd='2*int((nf+1)/2) * (W/nf + 0.29)' ps='2*int((nf+2)/2) * (W/nf + 0.29)' nrd='0.29 / W' nrs='0.29 / W'
+ sa=0 sb=0 sd=0 mult=1 m=1
XM5 out net2 AVDD AVDD sky130_fd_pr__pfet_01v8 L=1.0 W=1.0 nf=1 ad='int((nf+1)/2) * W/nf * 0.29' as='int((nf+2)/2) * W/nf * 0.29'
+ pd='2*int((nf+1)/2) * (W/nf + 0.29)' ps='2*int((nf+2)/2) * (W/nf + 0.29)' nrd='0.29 / W' nrs='0.29 / W'
+ sa=0 sb=0 sd=0 mult=1 m=1
XM4 net1 buf_n AGND AGND sky130_fd_pr__nfet_01v8 L=0.5 W=1.0 nf=1 ad='int((nf+1)/2) * W/nf * 0.29' as='int((nf+2)/2) * W/nf * 0.29'
+ pd='2*int((nf+1)/2) * (W/nf + 0.29)' ps='2*int((nf+2)/2) * (W/nf + 0.29)' nrd='0.29 / W' nrs='0.29 / W'
+ sa=0 sb=0 sd=0 mult=1 m=1
XM2 net2 mon net1 AGND sky130_fd_pr__nfet_01v8 L=0.5 W=1.0 nf=1 ad='int((nf+1)/2) * W/nf * 0.29' as='int((nf+2)/2) * W/nf * 0.29'
+ pd='2*int((nf+1)/2) * (W/nf + 0.29)' ps='2*int((nf+2)/2) * (W/nf + 0.29)' nrd='0.29 / W' nrs='0.29 / W'
+ sa=0 sb=0 sd=0 mult=1 m=1
XM3 out out net1 AGND sky130_fd_pr__nfet_01v8 L=0.5 W=1.0 nf=1 ad='int((nf+1)/2) * W/nf * 0.29' as='int((nf+2)/2) * W/nf * 0.29'
+ pd='2*int((nf+1)/2) * (W/nf + 0.29)' ps='2*int((nf+2)/2) * (W/nf + 0.29)' nrd='0.29 / W' nrs='0.29 / W'
+ sa=0 sb=0 sd=0 mult=1 m=1
.ends


* expanding   symbol:  schmitt_trigger.sym # of pins=4
** sym_path: design/xschem/schmitt_trigger.sym
** sch_path: design/xschem/schmitt_trigger.sch
.subckt schmitt_trigger A Y VDD GND
*.ipin A
*.opin Y
*.iopin VDD
*.iopin GND
XM3 net2 A GND GND sky130_fd_pr__nfet_01v8 L=0.15 W=0.65 nf=1 ad='int((nf+1)/2) * W/nf * 0.29' as='int((nf+2)/2) * W/nf * 0.29'
+ pd='2*int((nf+1)/2) * (W/nf + 0.29)' ps='2*int((nf+2)/2) * (W/nf + 0.29)' nrd='0.29 / W' nrs='0.29 / W'
+ sa=0 sb=0 sd=0 mult=1 m=1
XM1 Y A net2 GND sky130_fd_pr__nfet_01v8 L=0.15 W=0.65 nf=1 ad='int((nf+1)/2) * W/nf * 0.29' as='int((nf+2)/2) * W/nf * 0.29'
+ pd='2*int((nf+1)/2) * (W/nf + 0.29)' ps='2*int((nf+2)/2) * (W/nf + 0.29)' nrd='0.29 / W' nrs='0.29 / W'
+ sa=0 sb=0 sd=0 mult=1 m=1
XM7 VDD Y net2 GND sky130_fd_pr__nfet_01v8 L=0.15 W=0.42 nf=1 ad='int((nf+1)/2) * W/nf * 0.29' as='int((nf+2)/2) * W/nf * 0.29'
+ pd='2*int((nf+1)/2) * (W/nf + 0.29)' ps='2*int((nf+2)/2) * (W/nf + 0.29)' nrd='0.29 / W' nrs='0.29 / W'
+ sa=0 sb=0 sd=0 mult=1 m=1
XM4 net1 A VDD VDD sky130_fd_pr__pfet_01v8 L=0.15 W=1 nf=1 ad='int((nf+1)/2) * W/nf * 0.29' as='int((nf+2)/2) * W/nf * 0.29'
+ pd='2*int((nf+1)/2) * (W/nf + 0.29)' ps='2*int((nf+2)/2) * (W/nf + 0.29)' nrd='0.29 / W' nrs='0.29 / W'
+ sa=0 sb=0 sd=0 mult=1 m=1
XM2 Y A net1 VDD sky130_fd_pr__pfet_01v8 L=0.15 W=1 nf=1 ad='int((nf+1)/2) * W/nf * 0.29' as='int((nf+2)/2) * W/nf * 0.29'
+ pd='2*int((nf+1)/2) * (W/nf + 0.29)' ps='2*int((nf+2)/2) * (W/nf + 0.29)' nrd='0.29 / W' nrs='0.29 / W'
+ sa=0 sb=0 sd=0 mult=1 m=1
XM5 GND Y net1 VDD sky130_fd_pr__pfet_01v8 L=0.15 W=0.82 nf=1 ad='int((nf+1)/2) * W/nf * 0.29' as='int((nf+2)/2) * W/nf * 0.29'
+ pd='2*int((nf+1)/2) * (W/nf + 0.29)' ps='2*int((nf+2)/2) * (W/nf + 0.29)' nrd='0.29 / W' nrs='0.29 / W'
+ sa=0 sb=0 sd=0 mult=1 m=1
.ends


* expanding   symbol:  synapse_4bit_memory.sym # of pins=11
** sym_path: design/xschem/synapse_4bit_memory.sym
** sch_path: design/xschem/synapse_4bit_memory.sch
.subckt synapse_4bit_memory sout vstddpin spk resetW vthrdpin setW vtaudpip W[0] W[1] W[2] W[3]
+ vpulseextp GND VDD
*.iopin GND
*.iopin VDD
*.ipin vpulseextp
*.ipin spk
*.ipin vthrdpin
*.ipin vtaudpip
*.ipin vstddpin
*.ipin W[0],W[1],W[2],W[3]
*.ipin setW
*.ipin resetW
*.iopin sout
x1 vpulseextp spk GND spke VDD spike_extender
x3 vtaudpip sout vthrdpin spke vstddpin GND VDD net1[3] net1[2] net1[1] net1[0] dpi_syn_exc_4bit_fc
x2[0] setW W[0] net2 GND GND VDD VDD net1[3] sky130_fd_sc_hd__dfrtp_1
x2[1] setW W[1] net2 GND GND VDD VDD net1[2] sky130_fd_sc_hd__dfrtp_1
x2[2] setW W[2] net2 GND GND VDD VDD net1[1] sky130_fd_sc_hd__dfrtp_1
x2[3] setW W[3] net2 GND GND VDD VDD net1[0] sky130_fd_sc_hd__dfrtp_1
x11 resetW GND GND VDD VDD net2 sky130_fd_sc_hd__inv_1
.ends


* expanding   symbol:  decoder_4_to_16.sym # of pins=6
** sym_path: design/xschem/decoder_4_to_16.sym
** sch_path: design/xschem/decoder_4_to_16.sch
.subckt decoder_4_to_16 A[0] A[1] A[2] A[3] D[0] D[1] D[2] D[3] D[4] D[5] D[6] D[7] D[8] D[9] D[10]
+ D[11] D[12] D[13] D[14] D[15] req req_syn dVDD dGND
*.ipin A[0],A[1],A[2],A[3]
*.ipin req
*.opin D[0],D[1],D[2],D[3],D[4],D[5],D[6],D[7],D[8],D[9],D[10],D[11],D[12],D[13],D[14],D[15]
*.opin req_syn
*.iopin dVDD
*.iopin dGND
x21 req dGND dGND dVDD dVDD net5 sky130_fd_sc_hd__inv_1
x22 net5 dGND dGND dVDD dVDD net6 sky130_fd_sc_hd__inv_1
x23 net6 dGND dGND dVDD dVDD net7 sky130_fd_sc_hd__inv_1
x24 net7 dGND dGND dVDD dVDD req_syn sky130_fd_sc_hd__inv_1
x20 A[3] A[2] A[1] A[0] dGND dGND dVDD dVDD D[15] sky130_fd_sc_hd__and4_1
x19 A[3] A[2] A[1] net4 dGND dGND dVDD dVDD D[14] sky130_fd_sc_hd__and4_1
x18 A[3] A[2] net3 A[0] dGND dGND dVDD dVDD D[13] sky130_fd_sc_hd__and4_1
x17 A[3] A[2] net3 net4 dGND dGND dVDD dVDD D[12] sky130_fd_sc_hd__and4_1
x16 A[3] net2 A[1] A[0] dGND dGND dVDD dVDD D[11] sky130_fd_sc_hd__and4_1
x15 A[3] net2 A[1] net4 dGND dGND dVDD dVDD D[10] sky130_fd_sc_hd__and4_1
x13 A[3] net2 net3 A[0] dGND dGND dVDD dVDD D[9] sky130_fd_sc_hd__and4_1
x4 A[3] net2 net3 net4 dGND dGND dVDD dVDD D[8] sky130_fd_sc_hd__and4_1
x5 net1 A[2] A[1] A[0] dGND dGND dVDD dVDD D[7] sky130_fd_sc_hd__and4_1
x6 net1 A[2] A[1] net4 dGND dGND dVDD dVDD D[6] sky130_fd_sc_hd__and4_1
x8 net1 A[2] net3 net4 dGND dGND dVDD dVDD D[4] sky130_fd_sc_hd__and4_1
x9 net1 net2 A[1] net4 dGND dGND dVDD dVDD D[2] sky130_fd_sc_hd__and4_1
x10 net1 net2 net3 net4 dGND dGND dVDD dVDD D[0] sky130_fd_sc_hd__and4_1
x11 net1 net2 net3 A[0] dGND dGND dVDD dVDD D[1] sky130_fd_sc_hd__and4_1
x12 net1 net2 A[1] A[0] dGND dGND dVDD dVDD D[3] sky130_fd_sc_hd__and4_1
x14 net1 A[2] net3 A[0] dGND dGND dVDD dVDD D[5] sky130_fd_sc_hd__and4_1
x1 A[3] dGND dGND dVDD dVDD net1 sky130_fd_sc_hd__inv_4
x2 A[2] dGND dGND dVDD dVDD net2 sky130_fd_sc_hd__inv_4
x3 A[1] dGND dGND dVDD dVDD net3 sky130_fd_sc_hd__inv_4
x7 A[0] dGND dGND dVDD dVDD net4 sky130_fd_sc_hd__inv_4
.ends


* expanding   symbol:  synapse_4bit_memory_inh.sym # of pins=11
** sym_path: design/xschem/synapse_4bit_memory_inh.sym
** sch_path: design/xschem/synapse_4bit_memory_inh.sch
.subckt synapse_4bit_memory_inh sout vstddpip spk resetW vthrdpip setW vtaudpin W[0] W[1] W[2] W[3]
+ vpulseextp GND VDD
*.iopin GND
*.iopin VDD
*.ipin vpulseextp
*.ipin spk
*.ipin vthrdpip
*.ipin vtaudpin
*.ipin vstddpip
*.ipin W[0],W[1],W[2],W[3]
*.ipin setW
*.ipin resetW
*.iopin sout
x1 vpulseextp spk GND spke VDD spike_extender
x11 resetW GND GND VDD VDD net1 sky130_fd_sc_hd__inv_1
x3 vstddpip net2 net2 net2 net2 spke sout vthrdpip vtaudpin GND VDD dpi_syn_inh_4bit_fc
x2 setW W[0] net1 GND GND VDD VDD net3 net2 sky130_fd_sc_hd__dfrbp_1
.ends


* expanding   symbol:  spike_extender.sym # of pins=5
** sym_path: design/xschem/spike_extender.sym
** sch_path: design/xschem/spike_extender.sch
.subckt spike_extender vpulseextp spk GND spkext VDD
*.iopin GND
*.iopin VDD
*.ipin spk
*.opin spkext
*.ipin vpulseextp
XM1 net1 spk GND GND sky130_fd_pr__nfet_01v8 L=0.15 W=0.65 nf=1 ad='int((nf+1)/2) * W/nf * 0.29' as='int((nf+2)/2) * W/nf * 0.29'
+ pd='2*int((nf+1)/2) * (W/nf + 0.29)' ps='2*int((nf+2)/2) * (W/nf + 0.29)' nrd='0.29 / W' nrs='0.29 / W'
+ sa=0 sb=0 sd=0 mult=1 m=1
XM6 net1 vpulseextp VDD VDD sky130_fd_pr__pfet_01v8 L=2 W=1 nf=1 ad='int((nf+1)/2) * W/nf * 0.29' as='int((nf+2)/2) * W/nf * 0.29'
+ pd='2*int((nf+1)/2) * (W/nf + 0.29)' ps='2*int((nf+2)/2) * (W/nf + 0.29)' nrd='0.29 / W' nrs='0.29 / W'
+ sa=0 sb=0 sd=0 mult=1 m=1
XM5 net3 net2 GND GND sky130_fd_pr__nfet_01v8 L=0.15 W=0.65 nf=1 ad='int((nf+1)/2) * W/nf * 0.29' as='int((nf+2)/2) * W/nf * 0.29'
+ pd='2*int((nf+1)/2) * (W/nf + 0.29)' ps='2*int((nf+2)/2) * (W/nf + 0.29)' nrd='0.29 / W' nrs='0.29 / W'
+ sa=0 sb=0 sd=0 mult=1 m=1
XM8 spkext net3 GND GND sky130_fd_pr__nfet_01v8 L=0.15 W=0.65 nf=1 ad='int((nf+1)/2) * W/nf * 0.29' as='int((nf+2)/2) * W/nf * 0.29'
+ pd='2*int((nf+1)/2) * (W/nf + 0.29)' ps='2*int((nf+2)/2) * (W/nf + 0.29)' nrd='0.29 / W' nrs='0.29 / W'
+ sa=0 sb=0 sd=0 mult=1 m=1
XM4 net3 net2 VDD VDD sky130_fd_pr__pfet_01v8 L=0.15 W=1.0 nf=1 ad='int((nf+1)/2) * W/nf * 0.29' as='int((nf+2)/2) * W/nf * 0.29'
+ pd='2*int((nf+1)/2) * (W/nf + 0.29)' ps='2*int((nf+2)/2) * (W/nf + 0.29)' nrd='0.29 / W' nrs='0.29 / W'
+ sa=0 sb=0 sd=0 mult=1 m=1
XM7 spkext net3 VDD VDD sky130_fd_pr__pfet_01v8 L=0.15 W=1.0 nf=1 ad='int((nf+1)/2) * W/nf * 0.29' as='int((nf+2)/2) * W/nf * 0.29'
+ pd='2*int((nf+1)/2) * (W/nf + 0.29)' ps='2*int((nf+2)/2) * (W/nf + 0.29)' nrd='0.29 / W' nrs='0.29 / W'
+ sa=0 sb=0 sd=0 mult=1 m=1
XM2 net2 net1 GND GND sky130_fd_pr__nfet_01v8 L=0.15 W=0.65 nf=1 ad='int((nf+1)/2) * W/nf * 0.29' as='int((nf+2)/2) * W/nf * 0.29'
+ pd='2*int((nf+1)/2) * (W/nf + 0.29)' ps='2*int((nf+2)/2) * (W/nf + 0.29)' nrd='0.29 / W' nrs='0.29 / W'
+ sa=0 sb=0 sd=0 mult=1 m=1
XM3 net2 net1 VDD VDD sky130_fd_pr__pfet_01v8 L=0.15 W=1.0 nf=1 ad='int((nf+1)/2) * W/nf * 0.29' as='int((nf+2)/2) * W/nf * 0.29'
+ pd='2*int((nf+1)/2) * (W/nf + 0.29)' ps='2*int((nf+2)/2) * (W/nf + 0.29)' nrd='0.29 / W' nrs='0.29 / W'
+ sa=0 sb=0 sd=0 mult=1 m=1
XM9 GND net1 GND GND sky130_fd_pr__nfet_01v8 L=1 W=0.65 nf=1 ad='int((nf+1)/2) * W/nf * 0.29' as='int((nf+2)/2) * W/nf * 0.29'
+ pd='2*int((nf+1)/2) * (W/nf + 0.29)' ps='2*int((nf+2)/2) * (W/nf + 0.29)' nrd='0.29 / W' nrs='0.29 / W'
+ sa=0 sb=0 sd=0 mult=1 m=1
.ends


* expanding   symbol:  dpi_syn_exc_4bit_fc.sym # of pins=8
** sym_path: design/xschem/dpi_syn_exc_4bit_fc.sym
** sch_path: design/xschem/dpi_syn_exc_4bit_fc.sch
.subckt dpi_syn_exc_4bit_fc vtau sout vthn spk vstdn GND VDD weight[0] weight[1] weight[2] weight[3]
*.iopin GND
*.iopin VDD
*.iopin vtau
*.iopin vstdn
*.ipin spk
*.opin sout
*.iopin vthn
*.ipin weight[0],weight[1],weight[2],weight[3]
XM2 net3 spk net1 GND sky130_fd_pr__nfet_01v8 L=0.25 W=0.8 nf=1 ad='int((nf+1)/2) * W/nf * 0.29' as='int((nf+2)/2) * W/nf * 0.29'
+ pd='2*int((nf+1)/2) * (W/nf + 0.29)' ps='2*int((nf+2)/2) * (W/nf + 0.29)' nrd='0.29 / W' nrs='0.29 / W'
+ sa=0 sb=0 sd=0 mult=1 m=1
XC1 vsin VDD sky130_fd_pr__cap_mim_m3_1 W=5 L=5 MF=1 m=1
XM5 vsin vtau VDD VDD sky130_fd_pr__pfet_01v8 L=0.2 W=1.2 nf=1 ad='int((nf+1)/2) * W/nf * 0.29' as='int((nf+2)/2) * W/nf * 0.29'
+ pd='2*int((nf+1)/2) * (W/nf + 0.29)' ps='2*int((nf+2)/2) * (W/nf + 0.29)' nrd='0.29 / W' nrs='0.29 / W'
+ sa=0 sb=0 sd=0 mult=1 m=1
XM6 sout vsin VDD VDD sky130_fd_pr__pfet_01v8 L=0.2 W=1.2 nf=1 ad='int((nf+1)/2) * W/nf * 0.29' as='int((nf+2)/2) * W/nf * 0.29'
+ pd='2*int((nf+1)/2) * (W/nf + 0.29)' ps='2*int((nf+2)/2) * (W/nf + 0.29)' nrd='0.29 / W' nrs='0.29 / W'
+ sa=0 sb=0 sd=0 mult=1 m=1
XM1 net1 vstdn net2 GND sky130_fd_pr__nfet_01v8 L=0.5 W=0.8 nf=1 ad='int((nf+1)/2) * W/nf * 0.29' as='int((nf+2)/2) * W/nf * 0.29'
+ pd='2*int((nf+1)/2) * (W/nf + 0.29)' ps='2*int((nf+2)/2) * (W/nf + 0.29)' nrd='0.29 / W' nrs='0.29 / W'
+ sa=0 sb=0 sd=0 mult=1 m=1
XM4 vsin vsin net3 GND sky130_fd_pr__nfet_01v8 L=0.25 W=0.8 nf=1 ad='int((nf+1)/2) * W/nf * 0.29' as='int((nf+2)/2) * W/nf * 0.29'
+ pd='2*int((nf+1)/2) * (W/nf + 0.29)' ps='2*int((nf+2)/2) * (W/nf + 0.29)' nrd='0.29 / W' nrs='0.29 / W'
+ sa=0 sb=0 sd=0 mult=1 m=1
XM3 VDD vthn net3 GND sky130_fd_pr__nfet_01v8 L=0.25 W=0.8 nf=1 ad='int((nf+1)/2) * W/nf * 0.29' as='int((nf+2)/2) * W/nf * 0.29'
+ pd='2*int((nf+1)/2) * (W/nf + 0.29)' ps='2*int((nf+2)/2) * (W/nf + 0.29)' nrd='0.29 / W' nrs='0.29 / W'
+ sa=0 sb=0 sd=0 mult=1 m=1
XM7 net1 vstdn net4 GND sky130_fd_pr__nfet_01v8 L=2.0 W=0.8 nf=1 ad='int((nf+1)/2) * W/nf * 0.29' as='int((nf+2)/2) * W/nf * 0.29'
+ pd='2*int((nf+1)/2) * (W/nf + 0.29)' ps='2*int((nf+2)/2) * (W/nf + 0.29)' nrd='0.29 / W' nrs='0.29 / W'
+ sa=0 sb=0 sd=0 mult=1 m=1
XM8 net1 vstdn net5 GND sky130_fd_pr__nfet_01v8 L=4.0 W=0.8 nf=1 ad='int((nf+1)/2) * W/nf * 0.29' as='int((nf+2)/2) * W/nf * 0.29'
+ pd='2*int((nf+1)/2) * (W/nf + 0.29)' ps='2*int((nf+2)/2) * (W/nf + 0.29)' nrd='0.29 / W' nrs='0.29 / W'
+ sa=0 sb=0 sd=0 mult=1 m=1
XM9 net1 vstdn net6 GND sky130_fd_pr__nfet_01v8 L=8.0 W=0.8 nf=1 ad='int((nf+1)/2) * W/nf * 0.29' as='int((nf+2)/2) * W/nf * 0.29'
+ pd='2*int((nf+1)/2) * (W/nf + 0.29)' ps='2*int((nf+2)/2) * (W/nf + 0.29)' nrd='0.29 / W' nrs='0.29 / W'
+ sa=0 sb=0 sd=0 mult=1 m=1
XM10 net2 weight[0] GND GND sky130_fd_pr__nfet_01v8 L=0.25 W=0.8 nf=1 ad='int((nf+1)/2) * W/nf * 0.29'
+ as='int((nf+2)/2) * W/nf * 0.29' pd='2*int((nf+1)/2) * (W/nf + 0.29)' ps='2*int((nf+2)/2) * (W/nf + 0.29)'
+ nrd='0.29 / W' nrs='0.29 / W' sa=0 sb=0 sd=0 mult=1 m=1
XM11 net4 weight[1] GND GND sky130_fd_pr__nfet_01v8 L=0.25 W=0.8 nf=1 ad='int((nf+1)/2) * W/nf * 0.29'
+ as='int((nf+2)/2) * W/nf * 0.29' pd='2*int((nf+1)/2) * (W/nf + 0.29)' ps='2*int((nf+2)/2) * (W/nf + 0.29)'
+ nrd='0.29 / W' nrs='0.29 / W' sa=0 sb=0 sd=0 mult=1 m=1
XM12 net5 weight[2] GND GND sky130_fd_pr__nfet_01v8 L=0.25 W=0.8 nf=1 ad='int((nf+1)/2) * W/nf * 0.29'
+ as='int((nf+2)/2) * W/nf * 0.29' pd='2*int((nf+1)/2) * (W/nf + 0.29)' ps='2*int((nf+2)/2) * (W/nf + 0.29)'
+ nrd='0.29 / W' nrs='0.29 / W' sa=0 sb=0 sd=0 mult=1 m=1
XM13 net6 weight[3] GND GND sky130_fd_pr__nfet_01v8 L=0.25 W=0.8 nf=1 ad='int((nf+1)/2) * W/nf * 0.29'
+ as='int((nf+2)/2) * W/nf * 0.29' pd='2*int((nf+1)/2) * (W/nf + 0.29)' ps='2*int((nf+2)/2) * (W/nf + 0.29)'
+ nrd='0.29 / W' nrs='0.29 / W' sa=0 sb=0 sd=0 mult=1 m=1
.ends


* expanding   symbol:  dpi_syn_inh_4bit_fc.sym # of pins=8
** sym_path: design/xschem/dpi_syn_inh_4bit_fc.sym
** sch_path: design/xschem/dpi_syn_inh_4bit_fc.sch
.subckt dpi_syn_inh_4bit_fc vstdp weight_b[0] weight_b[1] weight_b[2] weight_b[3] spk sout vthrdp
+ vtaun GND VDD
*.ipin spk
*.iopin vstdp
*.iopin vthrdp
*.iopin vtaun
*.iopin sout
*.iopin GND
*.iopin VDD
*.ipin weight_b[0],weight_b[1],weight_b[2],weight_b[3]
XM5 net2 net3 net1 VDD sky130_fd_pr__pfet_01v8 L=0.2 W=1.2 nf=1 ad='int((nf+1)/2) * W/nf * 0.29' as='int((nf+2)/2) * W/nf * 0.29'
+ pd='2*int((nf+1)/2) * (W/nf + 0.29)' ps='2*int((nf+2)/2) * (W/nf + 0.29)' nrd='0.29 / W' nrs='0.29 / W'
+ sa=0 sb=0 sd=0 mult=1 m=1
XM2 GND vthrdp net2 VDD sky130_fd_pr__pfet_01v8 L=0.2 W=1.2 nf=1 ad='int((nf+1)/2) * W/nf * 0.29' as='int((nf+2)/2) * W/nf * 0.29'
+ pd='2*int((nf+1)/2) * (W/nf + 0.29)' ps='2*int((nf+2)/2) * (W/nf + 0.29)' nrd='0.29 / W' nrs='0.29 / W'
+ sa=0 sb=0 sd=0 mult=1 m=1
XM3 vsin vsin net2 VDD sky130_fd_pr__pfet_01v8 L=0.2 W=1.2 nf=1 ad='int((nf+1)/2) * W/nf * 0.29' as='int((nf+2)/2) * W/nf * 0.29'
+ pd='2*int((nf+1)/2) * (W/nf + 0.29)' ps='2*int((nf+2)/2) * (W/nf + 0.29)' nrd='0.29 / W' nrs='0.29 / W'
+ sa=0 sb=0 sd=0 mult=1 m=1
XM4 vsin vtaun GND GND sky130_fd_pr__nfet_01v8 L=0.25 W=0.8 nf=1 ad='int((nf+1)/2) * W/nf * 0.29' as='int((nf+2)/2) * W/nf * 0.29'
+ pd='2*int((nf+1)/2) * (W/nf + 0.29)' ps='2*int((nf+2)/2) * (W/nf + 0.29)' nrd='0.29 / W' nrs='0.29 / W'
+ sa=0 sb=0 sd=0 mult=1 m=1
XM6 sout vsin net8 GND sky130_fd_pr__nfet_01v8 L=0.25 W=0.8 nf=1 ad='int((nf+1)/2) * W/nf * 0.29' as='int((nf+2)/2) * W/nf * 0.29'
+ pd='2*int((nf+1)/2) * (W/nf + 0.29)' ps='2*int((nf+2)/2) * (W/nf + 0.29)' nrd='0.29 / W' nrs='0.29 / W'
+ sa=0 sb=0 sd=0 mult=1 m=1
XM7 net3 spk GND GND sky130_fd_pr__nfet_01v8 L=0.25 W=0.8 nf=1 ad='int((nf+1)/2) * W/nf * 0.29' as='int((nf+2)/2) * W/nf * 0.29'
+ pd='2*int((nf+1)/2) * (W/nf + 0.29)' ps='2*int((nf+2)/2) * (W/nf + 0.29)' nrd='0.29 / W' nrs='0.29 / W'
+ sa=0 sb=0 sd=0 mult=1 m=1
XM8 net3 spk VDD VDD sky130_fd_pr__pfet_01v8 L=0.2 W=1.2 nf=1 ad='int((nf+1)/2) * W/nf * 0.29' as='int((nf+2)/2) * W/nf * 0.29'
+ pd='2*int((nf+1)/2) * (W/nf + 0.29)' ps='2*int((nf+2)/2) * (W/nf + 0.29)' nrd='0.29 / W' nrs='0.29 / W'
+ sa=0 sb=0 sd=0 mult=1 m=1
XC1 GND vsin sky130_fd_pr__cap_mim_m3_1 W=5 L=5 MF=1 m=1
XM9 net4 vstdp VDD VDD sky130_fd_pr__pfet_01v8 L=0.4 W=1.2 nf=1 ad='int((nf+1)/2) * W/nf * 0.29' as='int((nf+2)/2) * W/nf * 0.29'
+ pd='2*int((nf+1)/2) * (W/nf + 0.29)' ps='2*int((nf+2)/2) * (W/nf + 0.29)' nrd='0.29 / W' nrs='0.29 / W'
+ sa=0 sb=0 sd=0 mult=1 m=1
XM10 net1 weight_b[0] net4 VDD sky130_fd_pr__pfet_01v8 L=0.2 W=1.2 nf=1 ad='int((nf+1)/2) * W/nf * 0.29'
+ as='int((nf+2)/2) * W/nf * 0.29' pd='2*int((nf+1)/2) * (W/nf + 0.29)' ps='2*int((nf+2)/2) * (W/nf + 0.29)'
+ nrd='0.29 / W' nrs='0.29 / W' sa=0 sb=0 sd=0 mult=1 m=1
XM11 net1 weight_b[1] net5 VDD sky130_fd_pr__pfet_01v8 L=0.2 W=1.2 nf=1 ad='int((nf+1)/2) * W/nf * 0.29'
+ as='int((nf+2)/2) * W/nf * 0.29' pd='2*int((nf+1)/2) * (W/nf + 0.29)' ps='2*int((nf+2)/2) * (W/nf + 0.29)'
+ nrd='0.29 / W' nrs='0.29 / W' sa=0 sb=0 sd=0 mult=1 m=1
XM1 net5 vstdp VDD VDD sky130_fd_pr__pfet_01v8 L=1.5 W=1.2 nf=1 ad='int((nf+1)/2) * W/nf * 0.29' as='int((nf+2)/2) * W/nf * 0.29'
+ pd='2*int((nf+1)/2) * (W/nf + 0.29)' ps='2*int((nf+2)/2) * (W/nf + 0.29)' nrd='0.29 / W' nrs='0.29 / W'
+ sa=0 sb=0 sd=0 mult=1 m=1
XM12 net6 vstdp VDD VDD sky130_fd_pr__pfet_01v8 L=3.0 W=1.2 nf=1 ad='int((nf+1)/2) * W/nf * 0.29' as='int((nf+2)/2) * W/nf * 0.29'
+ pd='2*int((nf+1)/2) * (W/nf + 0.29)' ps='2*int((nf+2)/2) * (W/nf + 0.29)' nrd='0.29 / W' nrs='0.29 / W'
+ sa=0 sb=0 sd=0 mult=1 m=1
XM13 net7 vstdp VDD VDD sky130_fd_pr__pfet_01v8 L=6.0 W=1.2 nf=1 ad='int((nf+1)/2) * W/nf * 0.29' as='int((nf+2)/2) * W/nf * 0.29'
+ pd='2*int((nf+1)/2) * (W/nf + 0.29)' ps='2*int((nf+2)/2) * (W/nf + 0.29)' nrd='0.29 / W' nrs='0.29 / W'
+ sa=0 sb=0 sd=0 mult=1 m=1
XM14 net1 weight_b[2] net6 VDD sky130_fd_pr__pfet_01v8 L=0.2 W=1.2 nf=1 ad='int((nf+1)/2) * W/nf * 0.29'
+ as='int((nf+2)/2) * W/nf * 0.29' pd='2*int((nf+1)/2) * (W/nf + 0.29)' ps='2*int((nf+2)/2) * (W/nf + 0.29)'
+ nrd='0.29 / W' nrs='0.29 / W' sa=0 sb=0 sd=0 mult=1 m=1
XM15 net1 weight_b[3] net7 VDD sky130_fd_pr__pfet_01v8 L=0.2 W=1.2 nf=1 ad='int((nf+1)/2) * W/nf * 0.29'
+ as='int((nf+2)/2) * W/nf * 0.29' pd='2*int((nf+1)/2) * (W/nf + 0.29)' ps='2*int((nf+2)/2) * (W/nf + 0.29)'
+ nrd='0.29 / W' nrs='0.29 / W' sa=0 sb=0 sd=0 mult=1 m=1
Vmeas net8 GND 0
.save i(vmeas)
.ends

.end
